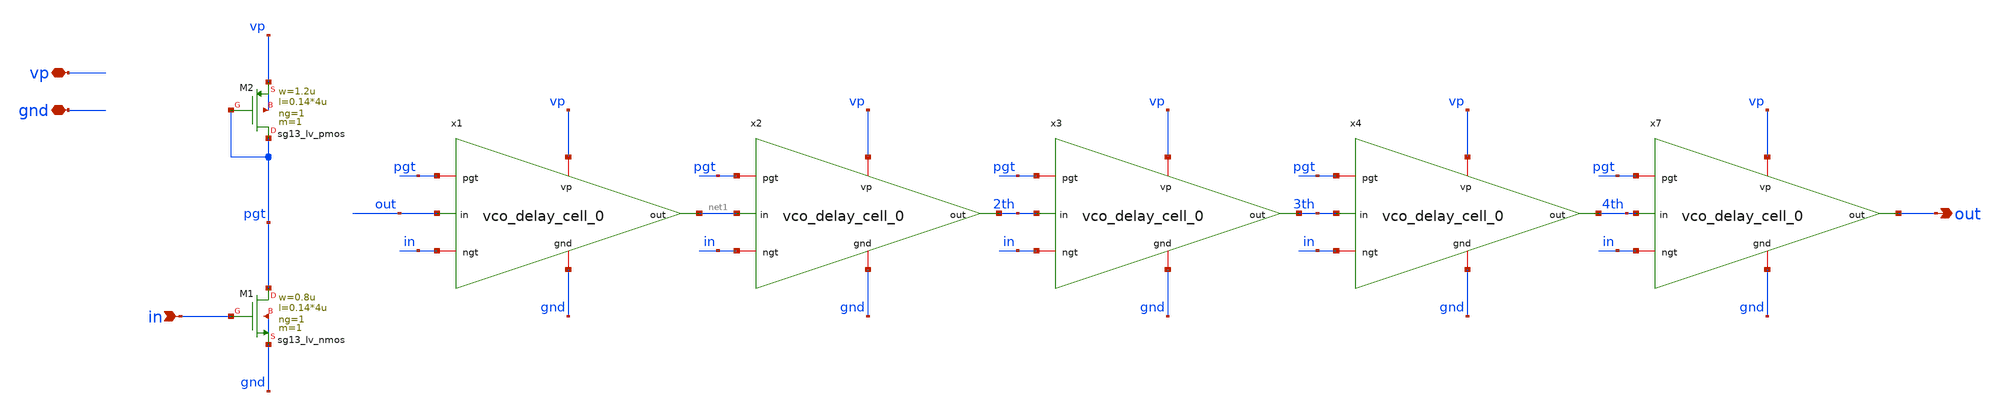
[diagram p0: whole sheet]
** sch_path: PLL0663-main/schematic/xschem/vco/vco_core_0.sch
**.subckt vco_core_0 in vp out gnd
*.ipin in
*.iopin vp
*.opin out
*.iopin gnd
XM1 pgt in gnd gnd sg13_lv_nmos w=0.8u l=0.14*4u ng=1 m=1 mm_ok=1
XM2 pgt pgt vp vp sg13_lv_pmos w=1.2u l=0.14*4u ng=1 m=1 mm_ok=1
x1 vp pgt out net1 in gnd vco_delay_cell_0
x2 vp pgt net1 2th in gnd vco_delay_cell_0
x3 vp pgt 2th 3th in gnd vco_delay_cell_0
x4 vp pgt 3th 4th in gnd vco_delay_cell_0
x7 vp pgt 4th out in gnd vco_delay_cell_0
**.ends

* expanding   symbol:  /foss/designs/CHIP-PLL/PLL0663-main/schematic/xschem/vco/vco_delay_cell_0.sym
*+ # of pins=6
** sym_path: schematics/vco/vco_cell/vco_delay_cell_0.sym
** sch_path: schematics/vco/vco_cell/vco_delay_cell_0.sch
.subckt vco_delay_cell_0 vp pgt in out ngt gnd
*.ipin in
*.opin out
*.iopin gnd
*.iopin vp
*.iopin pgt
*.iopin ngt
XM23 up pgt vp vp sg13_lv_pmos w=1.2u l=0.14*4u ng=1 m=1 mm_ok=1
XM1 out in up vp sg13_lv_pmos w=1.2u l=0.14*2u ng=1 m=1 mm_ok=1
XM2 out in dn gnd sg13_lv_nmos w=0.8u l=0.14*2u ng=1 m=1 mm_ok=1
XM26 dn ngt gnd gnd sg13_lv_nmos w=0.8u l=0.14*4u ng=1 m=1 mm_ok=1
.ends

.end
